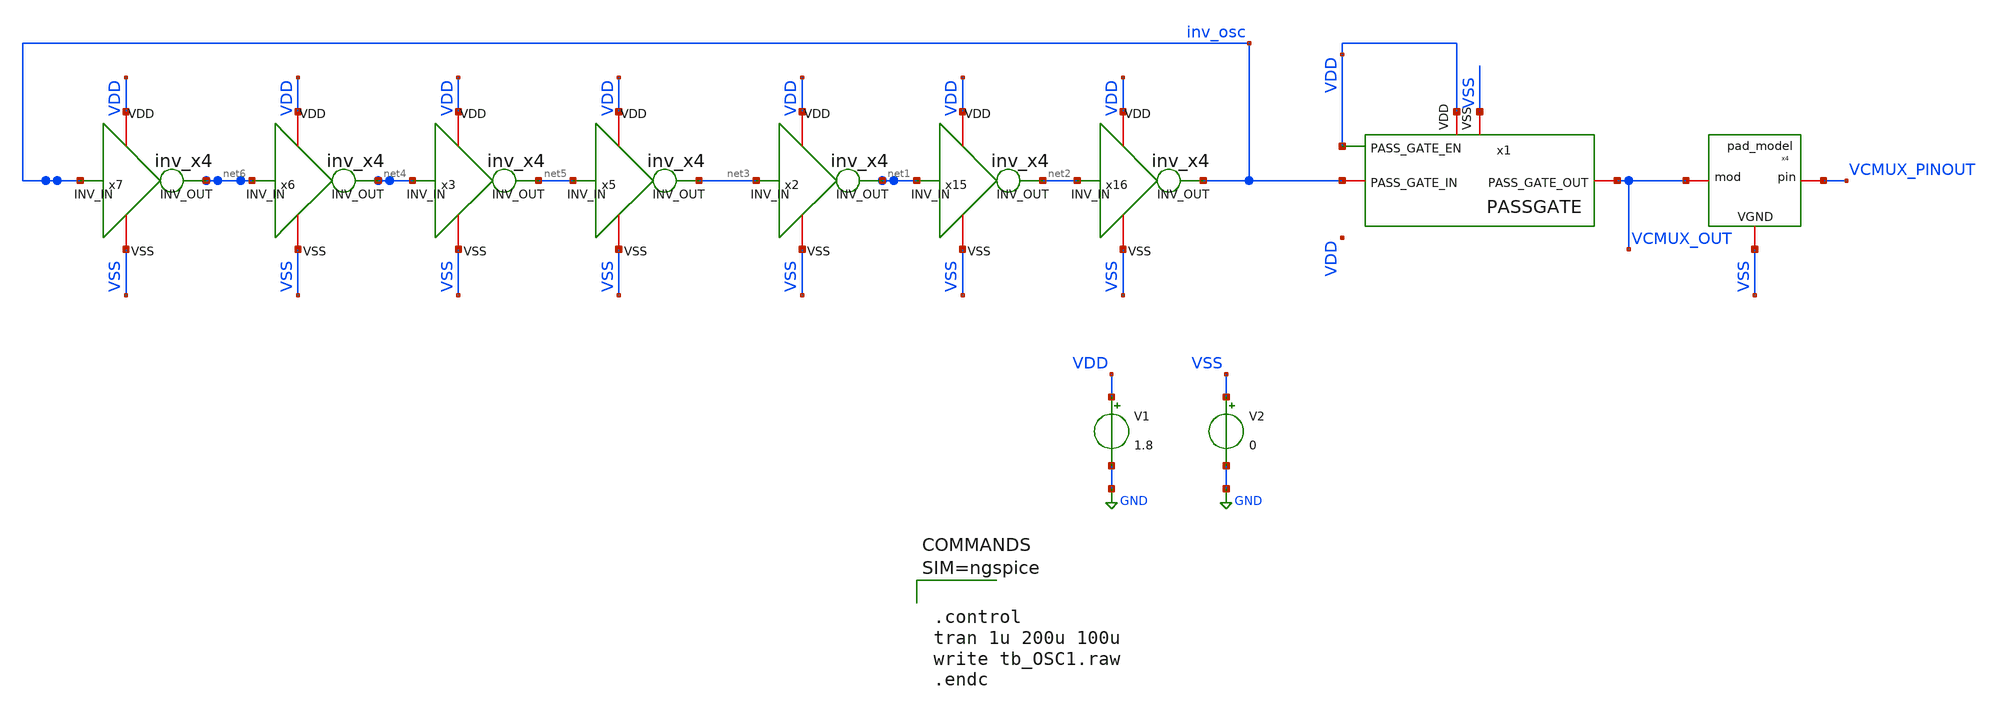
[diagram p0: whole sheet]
** sch_path: xschem/tb_OSC1.sch
**.subckt tb_OSC1
V1 VDD GND 1.8
V2 VSS GND 0
x4 VSS VCMUX_PINOUT VCMUX_OUT pad_model
x1 VDD inv_osc VSS VDD VCMUX_OUT PASSGATE
x15 VDD VSS net2 net1 inv_x4
x16 VDD VSS inv_osc net2 inv_x4
x2 VDD VSS net1 net3 inv_x4
x3 VDD VSS net5 net4 inv_x4
x5 VDD VSS net3 net5 inv_x4
x6 VDD VSS net4 net6 inv_x4
x7 VDD VSS net6 inv_osc inv_x4
**** begin user architecture code

** opencircuitdesign pdks install
.lib $::SKYWATER_MODELS/sky130.lib.spice tt





.control
tran 1u 200u 100u
write tb_OSC1.raw
.endc



**** end user architecture code
**.ends
.GLOBAL GND
.end
